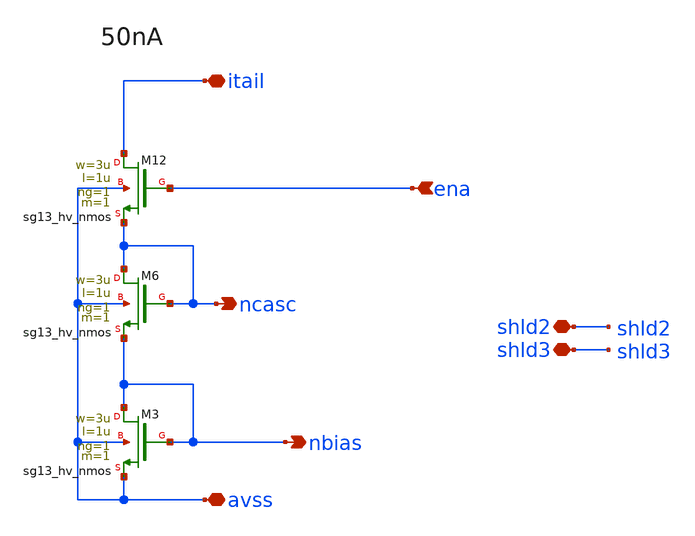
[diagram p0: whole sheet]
** sch_path: xschem/bias_nset.sch
**.subckt bias_nset avss ena itail nbias ncasc shld2 shld3
*.iopin avss
*.ipin ena
*.iopin itail
*.opin nbias
*.opin ncasc
*.iopin shld2
*.iopin shld3
XM3 nbias nbias avss avss sg13_hv_nmos w=3u l=1u ng=1 m=1 mm_ok=1
XM6 ncasc ncasc nbias avss sg13_hv_nmos w=3u l=1u ng=1 m=1 mm_ok=1
XM12 itail ena ncasc avss sg13_hv_nmos w=3u l=1u ng=1 m=1 mm_ok=1
**.ends
.end
